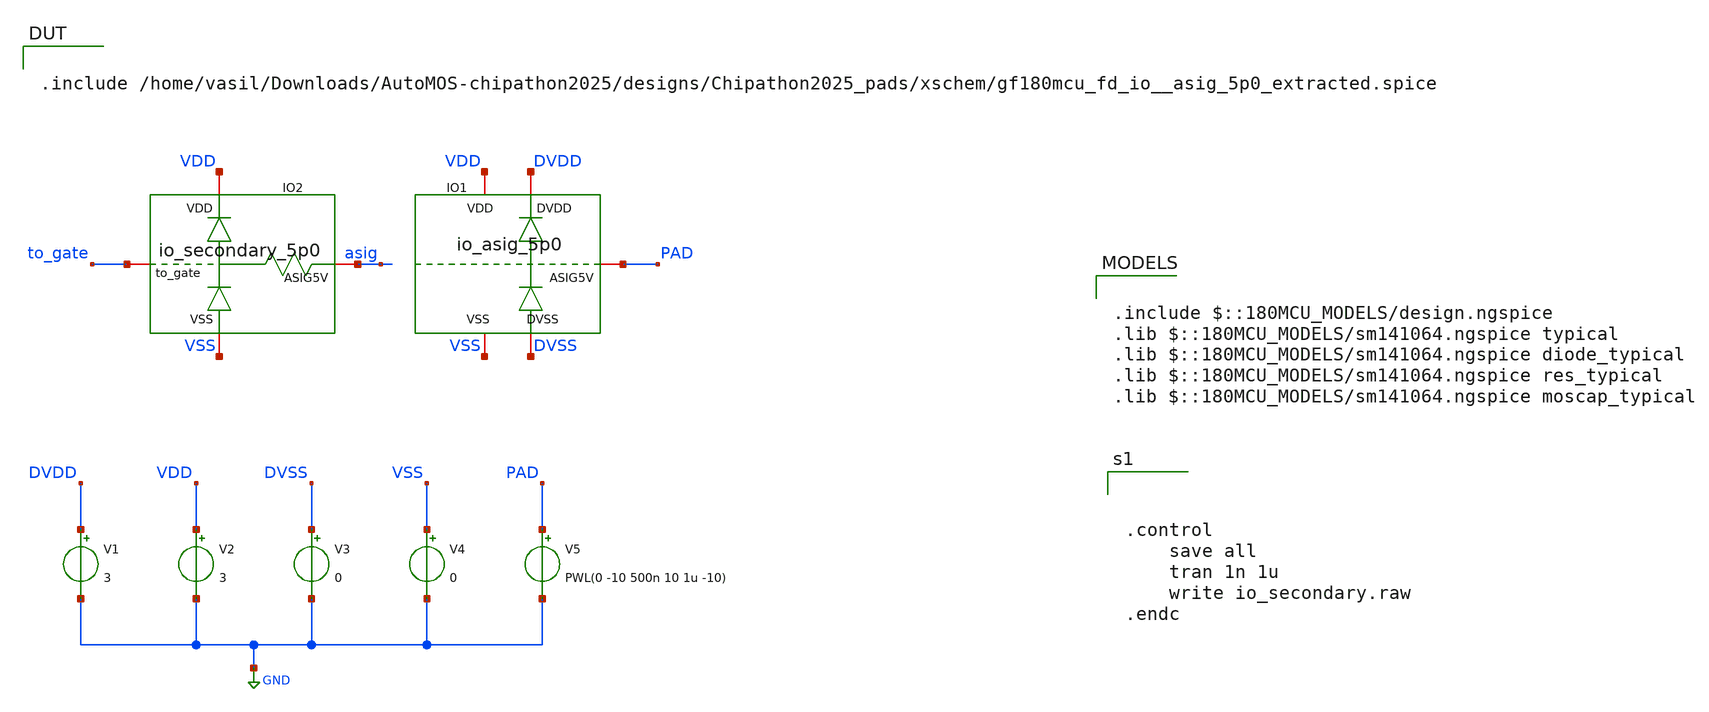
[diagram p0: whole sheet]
** sch_path: designs/Chipathon2025_pads/xschem/io_secondary_DC_tb.sch
**.subckt io_secondary_DC_tb
V1 DVDD GND 3
V2 VDD GND 3
V3 DVSS GND 0
V4 VSS GND 0
V5 PAD GND PWL(0 -10 500n 10 1u -10)
XIO1 PAD DVDD DVSS VDD VSS gf180mcu_fd_io__asig_5p0_extracted
XIO2 VDD to_gate asig VSS io_secondary_5p0
**** begin user architecture code

.include /home/vasil/Downloads/AutoMOS-chipathon2025/designs/Chipathon2025_pads/xschem/gf180mcu_fd_io__asig_5p0_extracted.spice


.include $::180MCU_MODELS/design.ngspice
.lib $::180MCU_MODELS/sm141064.ngspice typical
.lib $::180MCU_MODELS/sm141064.ngspice diode_typical
.lib $::180MCU_MODELS/sm141064.ngspice res_typical
.lib $::180MCU_MODELS/sm141064.ngspice moscap_typical




.control
    save all
    tran 1n 1u
    write io_secondary.raw
.endc


**** end user architecture code
**.ends

* expanding   symbol:  Chipathon2025_pads/xschem/symbols/io_asig_5p0.sym # of pins=5
** sym_path: designs/Chipathon2025_pads/xschem/symbols/io_asig_5p0.sym
.include /foss/designs/libs/Chipathon2025_pads/xschem/gf180mcu_fd_io.spice

* expanding   symbol:  Chipathon2025_pads/xschem/symbols/io_secondary_5p0/io_secondary_5p0.sym # of
*+ pins=4
** sym_path: Chipathon2025_pads/xschem/symbols/io_secondary_5p0/io_secondary_5p0.sym
** sch_path: Chipathon2025_pads/xschem/symbols/io_secondary_5p0/io_secondary_5p0.sch
.subckt io_secondary_5p0 VDD to_gate ASIG5V VSS


*.iopin VSS
*.iopin VDD
*.iopin to_gate
*.iopin ASIG5V
D1 to_gate VDD diode_pd2nw_06v0 area='10u * 10u ' pj='2*10u + 2*10u ' m=4
XR1 to_gate ASIG5V VDD ppolyf_u r_width=40e-6 r_length=10e-6 m=1
D2 VSS to_gate diode_nd2ps_06v0 area='10u * 10u ' pj='2*10u + 2*10u ' m=4
.ends

.GLOBAL GND
.end
